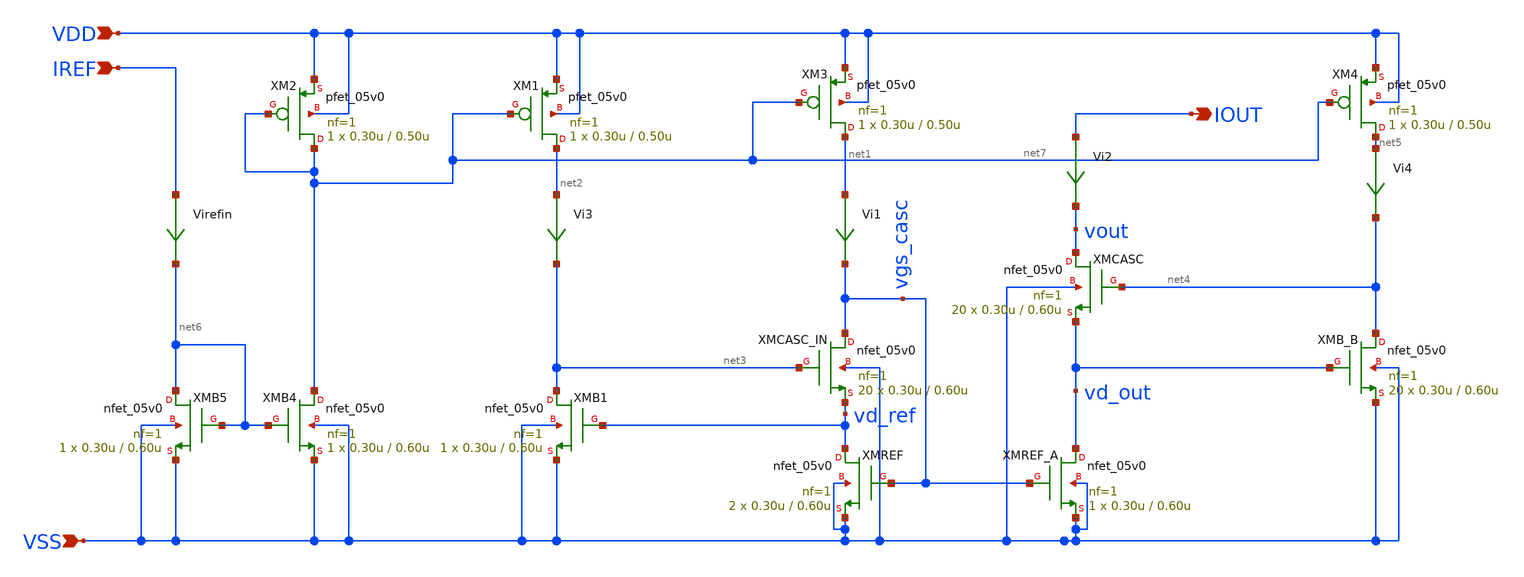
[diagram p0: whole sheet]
** sch_path: blocks/composite/regulated_cascoded_cmirror/Designs/design/cs-regulated-cascoded_5V.sch
**.subckt cs-regulated-cascoded_5V IOUT VDD VSS IREF
*.opin IOUT
*.ipin VDD
*.ipin VSS
*.ipin IREF
Vi1 net1 vgs_casc 0
.save i(vi1)
Vi2 IOUT vout 0
.save i(vi2)
Vi3 net2 net3 0
.save i(vi3)
Vi4 net5 net4 0
.save i(vi4)
Virefin IREF net6 0
.save i(virefin)
XMB5 net6 net6 VSS VSS nfet_05v0 L=0.60u W=0.30u nf=1 ad='int((nf+1)/2) * W/nf * 0.18u' as='int((nf+2)/2) * W/nf * 0.18u'
+ pd='2*int((nf+1)/2) * (W/nf + 0.18u)' ps='2*int((nf+2)/2) * (W/nf + 0.18u)' nrd='0.18u / W' nrs='0.18u / W'
+ sa=0 sb=0 sd=0 m=1
XMB4 net7 net6 VSS VSS nfet_05v0 L=0.60u W=0.30u nf=1 ad='int((nf+1)/2) * W/nf * 0.18u' as='int((nf+2)/2) * W/nf * 0.18u'
+ pd='2*int((nf+1)/2) * (W/nf + 0.18u)' ps='2*int((nf+2)/2) * (W/nf + 0.18u)' nrd='0.18u / W' nrs='0.18u / W'
+ sa=0 sb=0 sd=0 m=1
XMB1 net3 vd_ref VSS VSS nfet_05v0 L=0.60u W=0.30u nf=1 ad='int((nf+1)/2) * W/nf * 0.18u' as='int((nf+2)/2) * W/nf * 0.18u'
+ pd='2*int((nf+1)/2) * (W/nf + 0.18u)' ps='2*int((nf+2)/2) * (W/nf + 0.18u)' nrd='0.18u / W' nrs='0.18u / W'
+ sa=0 sb=0 sd=0 m=1
XMREF vd_ref vgs_casc VSS VSS nfet_05v0 L=0.60u W=0.30u nf=1 ad='int((nf+1)/2) * W/nf * 0.18u' as='int((nf+2)/2) * W/nf * 0.18u'
+ pd='2*int((nf+1)/2) * (W/nf + 0.18u)' ps='2*int((nf+2)/2) * (W/nf + 0.18u)' nrd='0.18u / W' nrs='0.18u / W'
+ sa=0 sb=0 sd=0 m=2
XMCASC_IN vgs_casc net3 vd_ref VSS nfet_05v0 L=0.60u W=0.30u nf=1 ad='int((nf+1)/2) * W/nf * 0.18u' as='int((nf+2)/2) * W/nf * 0.18u'
+ pd='2*int((nf+1)/2) * (W/nf + 0.18u)' ps='2*int((nf+2)/2) * (W/nf + 0.18u)' nrd='0.18u / W' nrs='0.18u / W'
+ sa=0 sb=0 sd=0 m=20
XMCASC vout net4 vd_out VSS nfet_05v0 L=0.60u W=0.30u nf=1 ad='int((nf+1)/2) * W/nf * 0.18u' as='int((nf+2)/2) * W/nf * 0.18u'
+ pd='2*int((nf+1)/2) * (W/nf + 0.18u)' ps='2*int((nf+2)/2) * (W/nf + 0.18u)' nrd='0.18u / W' nrs='0.18u / W'
+ sa=0 sb=0 sd=0 m=20
XMREF_A vd_out vgs_casc VSS VSS nfet_05v0 L=0.60u W=0.30u nf=1 ad='int((nf+1)/2) * W/nf * 0.18u' as='int((nf+2)/2) * W/nf * 0.18u'
+ pd='2*int((nf+1)/2) * (W/nf + 0.18u)' ps='2*int((nf+2)/2) * (W/nf + 0.18u)' nrd='0.18u / W' nrs='0.18u / W'
+ sa=0 sb=0 sd=0 m=1
XMB_B net4 vd_out VSS VSS nfet_05v0 L=0.60u W=0.30u nf=1 ad='int((nf+1)/2) * W/nf * 0.18u' as='int((nf+2)/2) * W/nf * 0.18u'
+ pd='2*int((nf+1)/2) * (W/nf + 0.18u)' ps='2*int((nf+2)/2) * (W/nf + 0.18u)' nrd='0.18u / W' nrs='0.18u / W'
+ sa=0 sb=0 sd=0 m=20
XM2 net7 net7 VDD VDD pfet_05v0 L=0.50u W=0.30u nf=1 ad='int((nf+1)/2) * W/nf * 0.18u' as='int((nf+2)/2) * W/nf * 0.18u'
+ pd='2*int((nf+1)/2) * (W/nf + 0.18u)' ps='2*int((nf+2)/2) * (W/nf + 0.18u)' nrd='0.18u / W' nrs='0.18u / W'
+ sa=0 sb=0 sd=0 m=1
XM1 net2 net7 VDD VDD pfet_05v0 L=0.50u W=0.30u nf=1 ad='int((nf+1)/2) * W/nf * 0.18u' as='int((nf+2)/2) * W/nf * 0.18u'
+ pd='2*int((nf+1)/2) * (W/nf + 0.18u)' ps='2*int((nf+2)/2) * (W/nf + 0.18u)' nrd='0.18u / W' nrs='0.18u / W'
+ sa=0 sb=0 sd=0 m=1
XM3 net1 net7 VDD VDD pfet_05v0 L=0.50u W=0.30u nf=1 ad='int((nf+1)/2) * W/nf * 0.18u' as='int((nf+2)/2) * W/nf * 0.18u'
+ pd='2*int((nf+1)/2) * (W/nf + 0.18u)' ps='2*int((nf+2)/2) * (W/nf + 0.18u)' nrd='0.18u / W' nrs='0.18u / W'
+ sa=0 sb=0 sd=0 m=1
XM4 net5 net7 VDD VDD pfet_05v0 L=0.50u W=0.30u nf=1 ad='int((nf+1)/2) * W/nf * 0.18u' as='int((nf+2)/2) * W/nf * 0.18u'
+ pd='2*int((nf+1)/2) * (W/nf + 0.18u)' ps='2*int((nf+2)/2) * (W/nf + 0.18u)' nrd='0.18u / W' nrs='0.18u / W'
+ sa=0 sb=0 sd=0 m=1
**.ends
.end
